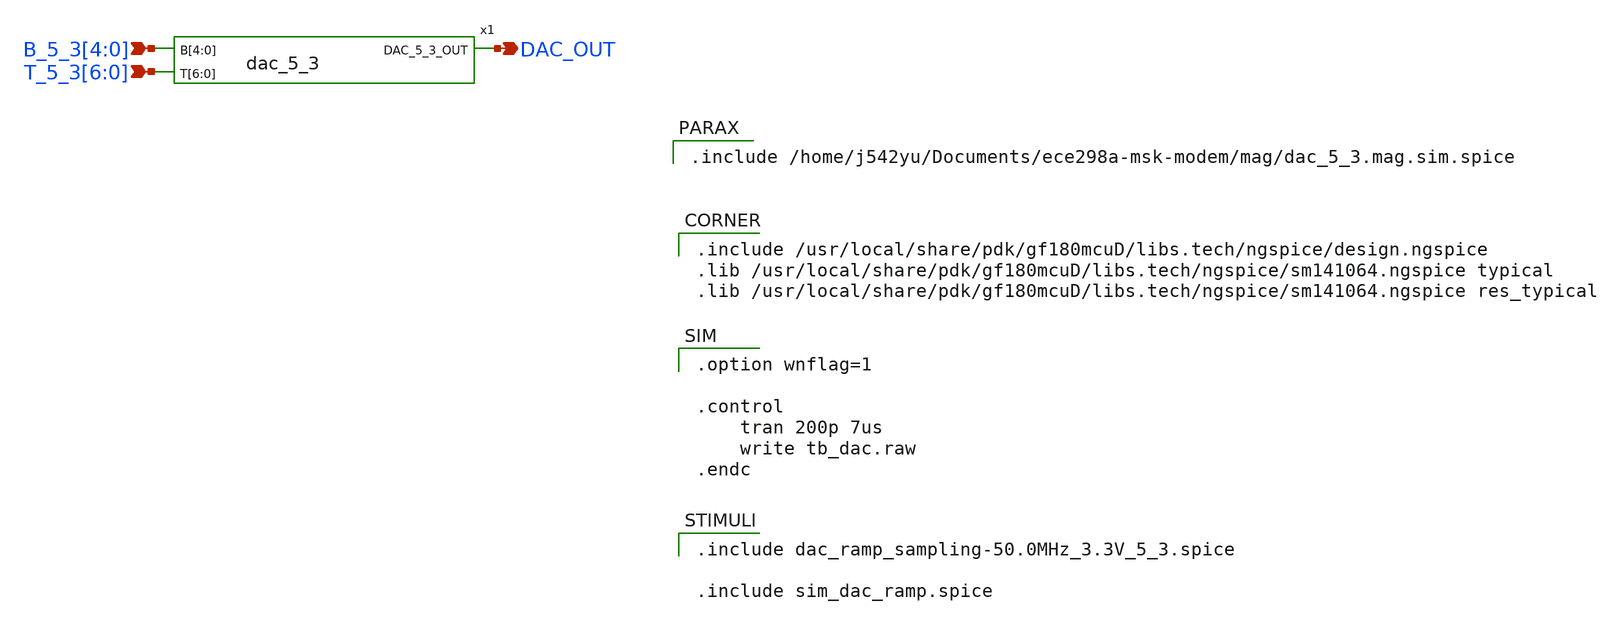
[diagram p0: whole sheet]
** sch_path: xschem/tb_dac.sch
**.subckt tb_dac B_5_3[4],B_5_3[3],B_5_3[2],B_5_3[1],B_5_3[0]
*+ T_5_3[6],T_5_3[5],T_5_3[4],T_5_3[3],T_5_3[2],T_5_3[1],T_5_3[0] DAC_OUT
*.ipin B_5_3[4],B_5_3[3],B_5_3[2],B_5_3[1],B_5_3[0]
*.ipin T_5_3[6],T_5_3[5],T_5_3[4],T_5_3[3],T_5_3[2],T_5_3[1],T_5_3[0]
*.opin DAC_OUT
x1 DAC_OUT B_5_3[4] B_5_3[3] B_5_3[2] B_5_3[1] B_5_3[0] T_5_3[6] T_5_3[5] T_5_3[4] T_5_3[3] T_5_3[2]
+ T_5_3[1] T_5_3[0] dac_5_3
**** begin user architecture code

.option wnflag=1

.control
    tran 200p 7us
    write tb_dac.raw
.endc



.include dac_ramp_sampling-50.0MHz_3.3V_5_3.spice

.include sim_dac_ramp.spice


.include /usr/local/share/pdk/gf180mcuD/libs.tech/ngspice/design.ngspice
.lib /usr/local/share/pdk/gf180mcuD/libs.tech/ngspice/sm141064.ngspice typical
.lib /usr/local/share/pdk/gf180mcuD/libs.tech/ngspice/sm141064.ngspice res_typical


.include /home/j542yu/Documents/ece298a-msk-modem/mag/dac_5_3.mag.sim.spice

**** end user architecture code
**.ends

* expanding   symbol:  dac_5_3.sym # of pins=3
** sym_path: xschem/dac_5_3.sym
** sch_path: xschem/dac_5_3.sch
.subckt dac_5_3 DAC_5_3_OUT B[4] B[3] B[2] B[1] B[0] T[6] T[5] T[4] T[3] T[2] T[1] T[0]
*.ipin B[4],B[3],B[2],B[1],B[0]
*.ipin T[6],T[5],T[4],T[3],T[2],T[1],T[0]
*.opin DAC_5_3_OUT
x1 net3 net1 B[0] dac_sub_r2r
x2 net4 net3 B[1] dac_sub_r2r
x3 net5 net4 B[2] dac_sub_r2r
x4 net6 net5 B[3] dac_sub_r2r
x5 DAC_5_3_OUT net6 B[4] dac_sub_r2r
* tap: B[4:0] --> B[0]
* tap: B[4:0] --> B[1]
* tap: B[4:0] --> B[2]
* tap: B[4:0] --> B[3]
* tap: B[4:0] --> B[4]
x6 DAC_5_3_OUT T[0] dac_sub_therm
x7 DAC_5_3_OUT T[1] dac_sub_therm
x8 DAC_5_3_OUT T[2] dac_sub_therm
x9 DAC_5_3_OUT T[3] dac_sub_therm
x10 DAC_5_3_OUT T[4] dac_sub_therm
x11 DAC_5_3_OUT T[5] dac_sub_therm
x12 DAC_5_3_OUT T[6] dac_sub_therm
* tap: T[6:0] --> T[0]
* tap: T[6:0] --> T[1]
* tap: T[6:0] --> T[2]
* tap: T[6:0] --> T[3]
* tap: T[6:0] --> T[4]
* tap: T[6:0] --> T[5]
* tap: T[6:0] --> T[6]
XR2 GND net7 GND ppolyf_u_1k r_width=2e-6 r_length=20e-6 m=1
XR3 net7 net1 GND ppolyf_u_1k r_width=2e-6 r_length=20e-6 m=1
XR4 GND net2 GND ppolyf_u_1k r_width=2e-6 r_length=20e-6 m=1
XR5 GND net2 GND ppolyf_u_1k r_width=2e-6 r_length=20e-6 m=1
XR7 GND net2 net8 ppolyf_u_1k r_width=2e-6 r_length=20e-6 m=1
.ends


* expanding   symbol:  dac_sub_r2r.sym # of pins=3
** sym_path: xschem/dac_sub_r2r.sym
** sch_path: xschem/dac_sub_r2r.sch
.subckt dac_sub_r2r R_node_out R_node_in in
*.ipin in
*.iopin R_node_out
*.iopin R_node_in
XR7 in net1 GND ppolyf_u_1k r_width=2e-6 r_length=20e-6 m=1
XR1 net1 R_node_in GND ppolyf_u_1k r_width=2e-6 r_length=20e-6 m=1
XR2 net2 R_node_in GND ppolyf_u_1k r_width=2e-6 r_length=20e-6 m=1
XR3 R_node_out net2 GND ppolyf_u_1k r_width=2e-6 r_length=20e-6 m=1
XR4 net3 R_node_in GND ppolyf_u_1k r_width=2e-6 r_length=20e-6 m=1
XR5 R_node_out net3 GND ppolyf_u_1k r_width=2e-6 r_length=20e-6 m=1
.ends


* expanding   symbol:  dac_sub_therm.sym # of pins=2
** sym_path: xschem/dac_sub_therm.sym
** sch_path: xschem/dac_sub_therm.sch
.subckt dac_sub_therm R_node in
*.ipin in
*.iopin R_node
XR7 in net1 GND ppolyf_u_1k r_width=2e-6 r_length=20e-6 m=1
XR1 net1 R_node GND ppolyf_u_1k r_width=2e-6 r_length=20e-6 m=1
.ends

.GLOBAL GND
.end
